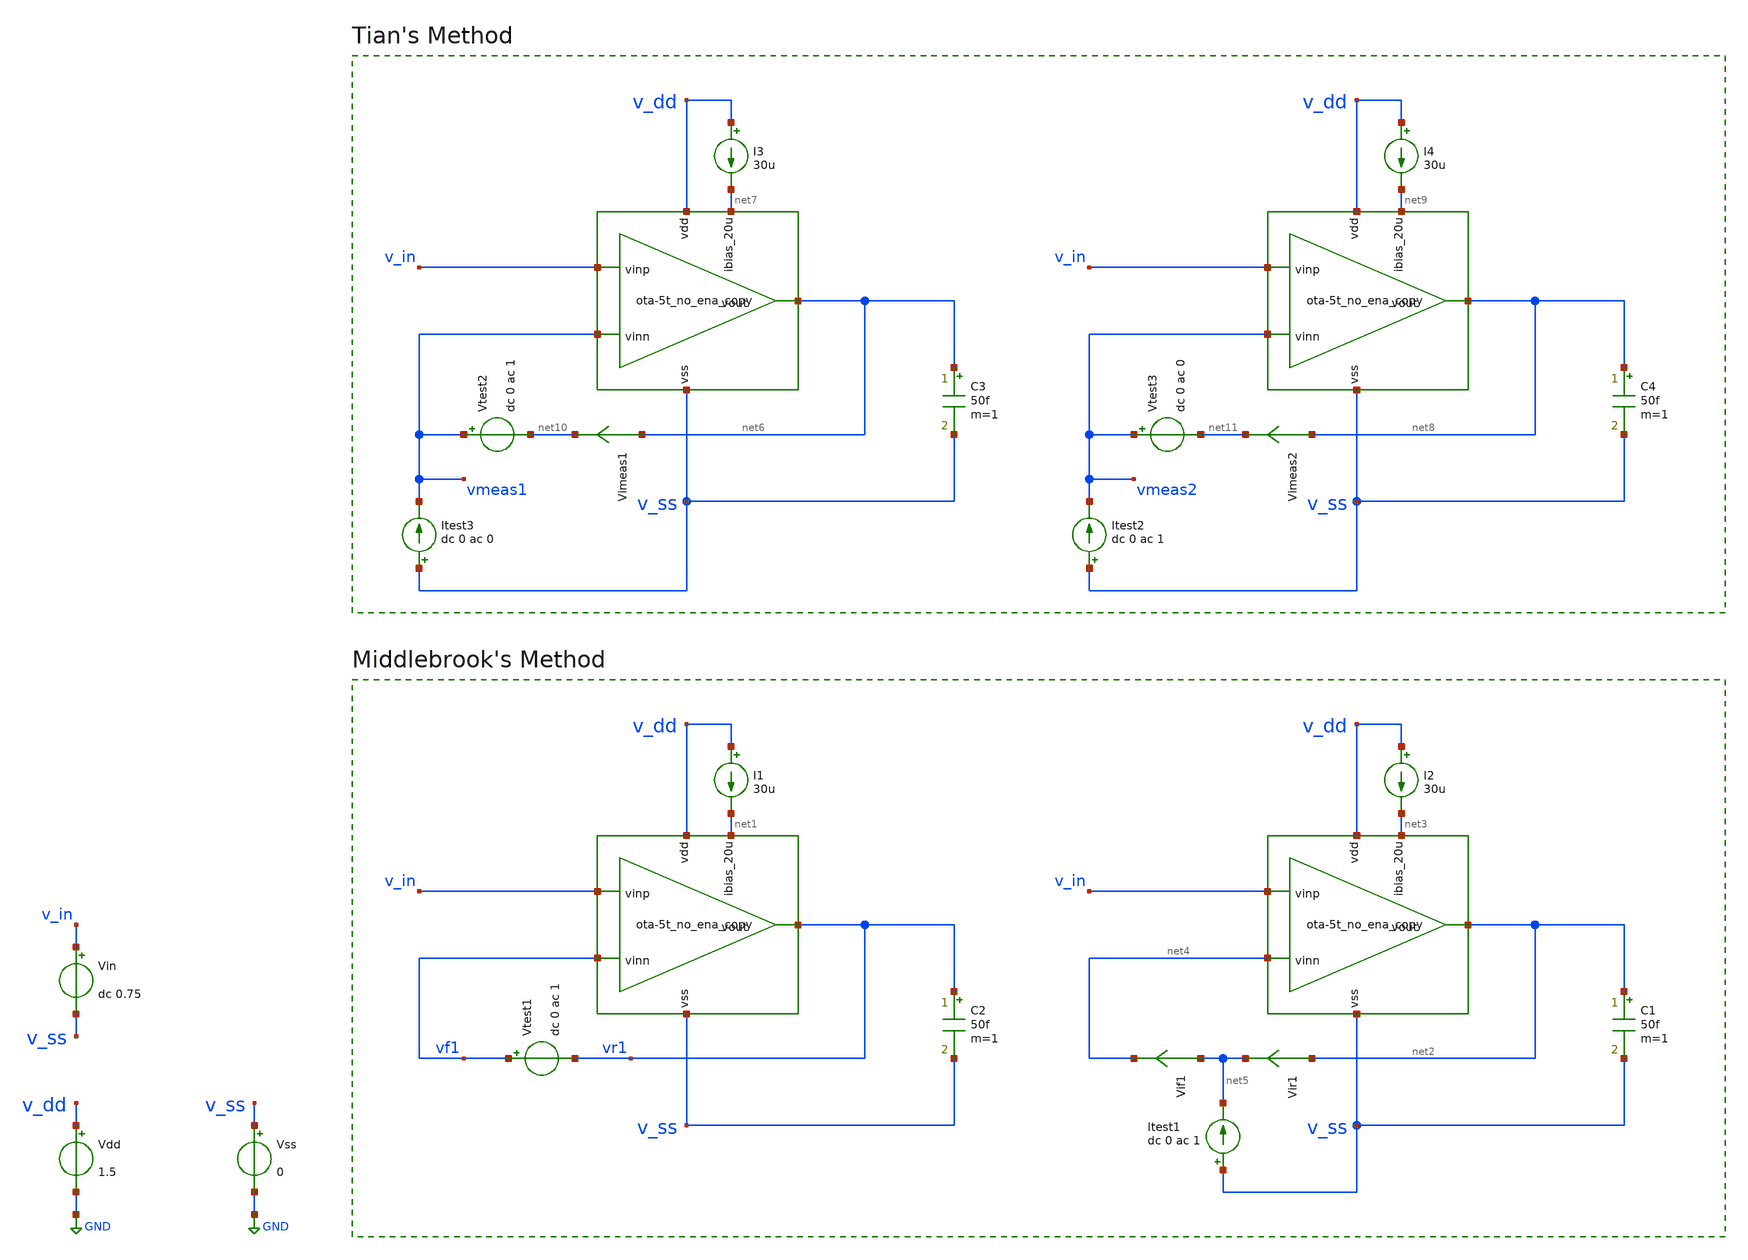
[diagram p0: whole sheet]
** sch_path: 004_Real_Circuits/004_testbench_ota_results/temperature_analysis/ota-5t_tb-loopgain_no_ena.sch
* (c) 2024-2025 H. Pretl, S. Dorrer, Apache-2.0 license
**.subckt ota-5t_tb-loopgain_no_ena
Vdd v_dd GND 1.5
Vss v_ss GND 0
Vin v_in v_ss dc 0.75
C2 vr1 v_ss 50f m=1
I1 v_dd net1 30u
Vtest1 vf1 vr1 dc 0 ac 1
C1 net2 v_ss 50f m=1
I2 v_dd net3 30u
Vir1 net2 net5 0
.save i(vir1)
Vif1 net5 net4 0
.save i(vif1)
Itest1 v_ss net5 dc 0 ac 1
C3 net6 v_ss 50f m=1
I3 v_dd net7 30u
C4 net8 v_ss 50f m=1
I4 v_dd net9 30u
Itest3 v_ss vmeas1 dc 0 ac 0
Vtest2 vmeas1 net10 dc 0 ac 1
Vimeas1 net6 net10 0
.save i(vimeas1)
Itest2 v_ss vmeas2 dc 0 ac 1
Vtest3 vmeas2 net11 dc 0 ac 0
Vimeas2 net8 net11 0
.save i(vimeas2)
x1 v_dd net6 v_in vmeas1 net7 v_ss ota-5t_no_ena_copy
x2 v_dd net8 v_in vmeas2 net9 v_ss ota-5t_no_ena_copy
x3 v_dd vr1 v_in vf1 net1 v_ss ota-5t_no_ena_copy
x4 v_dd net2 v_in net4 net3 v_ss ota-5t_no_ena_copy
**** begin user architecture code
 .lib cornerMOSlv.lib mos_tt



.param temp=27
.options savecurrents reltol=1e-3 abstol=1e-12 gmin=1e-15
.control
save all

foreach ti -40 -20 0 20 40 60 80 100 120 140
    option temp = $ti

    op
    ac dec 101 1 100G

    * Tian's Method
    * vtest=0, itest=1:
    let A=i(Vimeas2)
    let C=v(vmeas2)

    * vtest=1, itest=0:
    let B=i(Vimeas1)
    let D=v(vmeas1)
    let ttian=(A*D-B*C-A)/(2*(B*C-A*D)+A-D+1)

    wrdata out_ac_${ti}.txt v_out
end

plot db(ac1.ttian) db(ac2.ttian) db(ac3.ttian) db(ac4.ttian) db(ac5.ttian) db(ac6.ttian) db(ac7.ttian) db(ac8.ttian) db(ac9.ttian) ylabel 'Magnitude
+ - Tian'

plot 180/pi*cphase(ac1.ttian) 180/pi*cphase(ac2.ttian) 180/pi*cphase(ac3.ttian) 180/pi*cphase(ac4.ttian) 180/pi*cphase(ac5.ttian) 180/pi*cphase(ac6.ttian) 180/pi*cphase(ac7.ttian) 180/pi*cphase(ac8.ttian) 180/pi*cphase(ac9.ttian) ylabel 'Phase
+ - Tian'

.endc


**** end user architecture code
**.ends

* expanding   symbol:  003_version_second_output_stage/ota-5t_no_ena_copy.sym # of pins=6
** sym_path: 004_Real_Circuits/003_version_second_output_stage/ota-5t_no_ena_copy.sym
** sch_path: 004_Real_Circuits/003_version_second_output_stage/ota-5t_no_ena_copy.sch
.subckt ota-5t_no_ena_copy vdd vout vinp vinn ibias_20u vss
*.opin vout
*.iopin vdd
*.ipin vinp
*.ipin vinn
*.ipin ibias_20u
*.iopin vss
XM5 tail ibias_20u vss vss sg13_lv_nmos w=1.5u l=5u ng=1 m=1 mm_ok=1
XM4 net1 gate_p vdd vdd sg13_lv_pmos w=3.5u l=5u ng=1 m=1 mm_ok=1
XM1 gate_p vinn tail vss sg13_lv_nmos w=2u l=5u ng=1 m=1 mm_ok=1
XM2 net1 vinp tail vss sg13_lv_nmos w=2u l=5u ng=1 m=1 mm_ok=1
XM3 gate_p gate_p vdd vdd sg13_lv_pmos w=3.5u l=5u ng=1 m=1 mm_ok=1
XM6 ibias_20u ibias_20u vss vss sg13_lv_nmos w=10u l=5u ng=5 m=1 mm_ok=1
XM7 vout net1 vdd vdd sg13_lv_pmos w=8.5u l=5u ng=1 m=1 mm_ok=1
XM8 vout ibias_20u vss vss sg13_lv_nmos w=0.75u l=5u ng=1 m=1 mm_ok=1
C2 net2 vout 795f m=1
R1 net1 net2 59k m=1
.ends

.GLOBAL GND
.end
